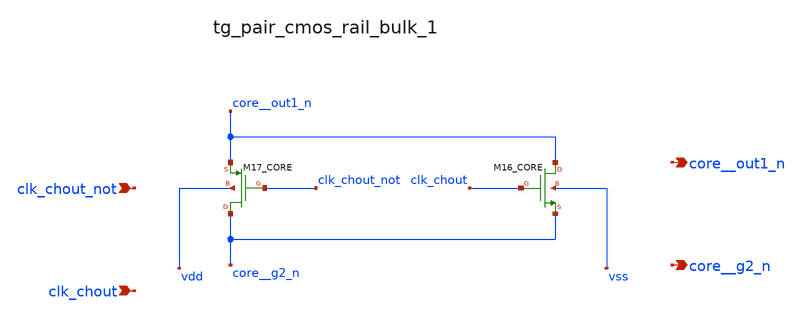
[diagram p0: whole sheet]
** sch_path: analog-db/raw/ia_006_fan_chopper_cmfb/hier/blocks/tg_pair_cmos_rail_bulk_1.sch
**.subckt tg_pair_cmos_rail_bulk_1 clk_chout_not clk_chout core__out1_n core__g2_n
*.ipin clk_chout_not
*.ipin clk_chout
*.opin core__out1_n
*.opin core__g2_n
XM16_CORE core__out1_n clk_chout core__g2_n vss sg13_lv_nmos w=x_dut_xm16_core_w l=x_dut_xm16_core_l
+ ng=1 m=x_dut_xm16_core_m
XM17_CORE core__g2_n clk_chout_not core__out1_n vdd sg13_lv_pmos w=x_dut_xm17_core_w
+ l=x_dut_xm17_core_l ng=1 m=x_dut_xm17_core_m
**.ends
.end
